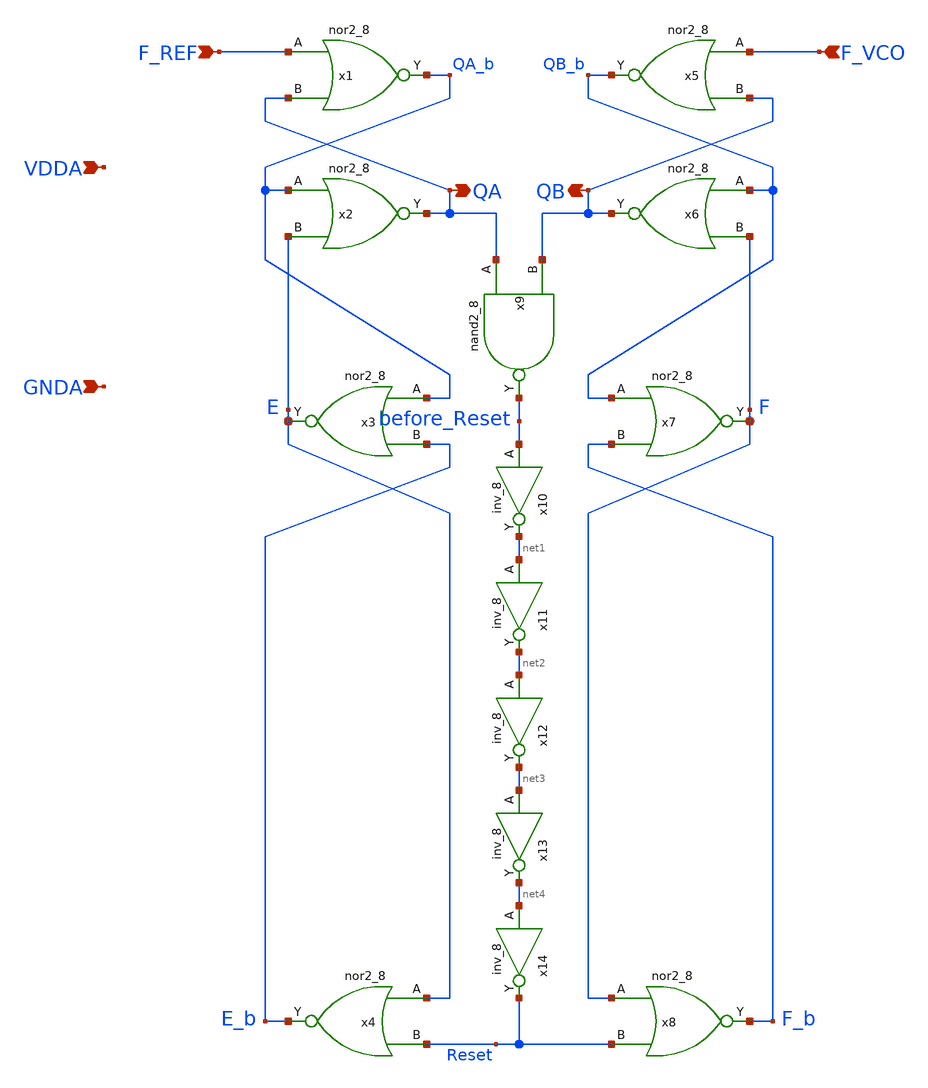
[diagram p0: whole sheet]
** sch_path: projects/pll/pfd/xschem_ngspice/phase_frequency_detector_2.sch
**.subckt phase_frequency_detector_2 F_REF QA F_VCO QB VDDA GNDA
*.ipin F_REF
*.opin QA
*.ipin F_VCO
*.opin QB
*.ipin VDDA
*.ipin GNDA
x1 F_REF QA GNDA GNDA VDDA VDDA QA_b sky130_fd_sc_hd__nor2_8
x2 QA_b E GNDA GNDA VDDA VDDA QA sky130_fd_sc_hd__nor2_8
x3 QA_b E_b GNDA GNDA VDDA VDDA E sky130_fd_sc_hd__nor2_8
x4 E Reset GNDA GNDA VDDA VDDA E_b sky130_fd_sc_hd__nor2_8
x5 F_VCO QB GNDA GNDA VDDA VDDA QB_b sky130_fd_sc_hd__nor2_8
x6 QB_b F GNDA GNDA VDDA VDDA QB sky130_fd_sc_hd__nor2_8
x7 QB_b F_b GNDA GNDA VDDA VDDA F sky130_fd_sc_hd__nor2_8
x8 F Reset GNDA GNDA VDDA VDDA F_b sky130_fd_sc_hd__nor2_8
x9 QA QB GNDA GNDA VDDA VDDA before_Reset sky130_fd_sc_hd__nand2_8
x10 before_Reset GNDA GNDA VDDA VDDA net1 sky130_fd_sc_hd__inv_8
x11 net1 GNDA GNDA VDDA VDDA net2 sky130_fd_sc_hd__inv_8
x12 net2 GNDA GNDA VDDA VDDA net3 sky130_fd_sc_hd__inv_8
x13 net3 GNDA GNDA VDDA VDDA net4 sky130_fd_sc_hd__inv_8
x14 net4 GNDA GNDA VDDA VDDA Reset sky130_fd_sc_hd__inv_8
**.ends
.end
